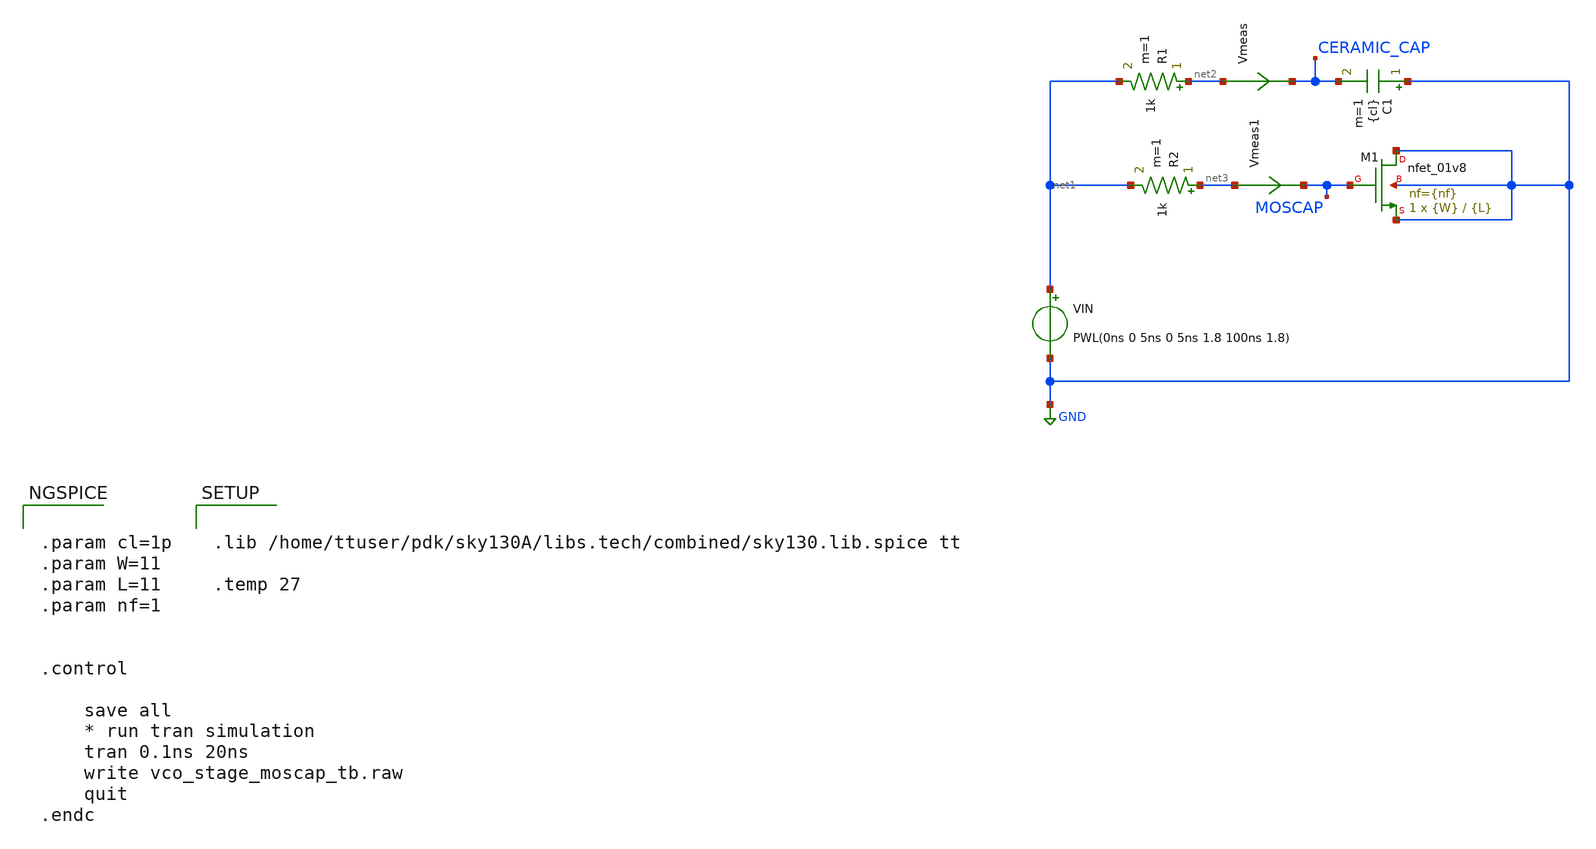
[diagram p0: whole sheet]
** sch_path: xschem/vco_stage_moscap_tb.sch
**.subckt vco_stage_moscap_tb
VIN net1 GND PWL(0ns 0 5ns 0 5ns 1.8 100ns 1.8)
R1 net2 net1 1k m=1
C1 GND CERAMIC_CAP {cl} m=1
Vmeas net2 CERAMIC_CAP 0
.save i(vmeas)
XM1 GND MOSCAP GND GND sky130_fd_pr__nfet_01v8 L={L} W={W} nf={nf} ad='int((nf+1)/2) * W/nf * 0.29' as='int((nf+2)/2) * W/nf * 0.29'
+ pd='2*int((nf+1)/2) * (W/nf + 0.29)' ps='2*int((nf+2)/2) * (W/nf + 0.29)' nrd='0.29 / W' nrs='0.29 / W'
+ sa=0 sb=0 sd=0 mult=1 m=1
R2 net3 net1 1k m=1
Vmeas1 net3 MOSCAP 0
.save i(vmeas1)
**** begin user architecture code


.param cl=1p
.param W=11
.param L=11
.param nf=1


.control

    save all
    * run tran simulation
    tran 0.1ns 20ns
    write vco_stage_moscap_tb.raw
    quit
.endc




.lib /home/ttuser/pdk/sky130A/libs.tech/combined/sky130.lib.spice tt

.temp 27


**** end user architecture code
**.ends
.GLOBAL GND
.end
